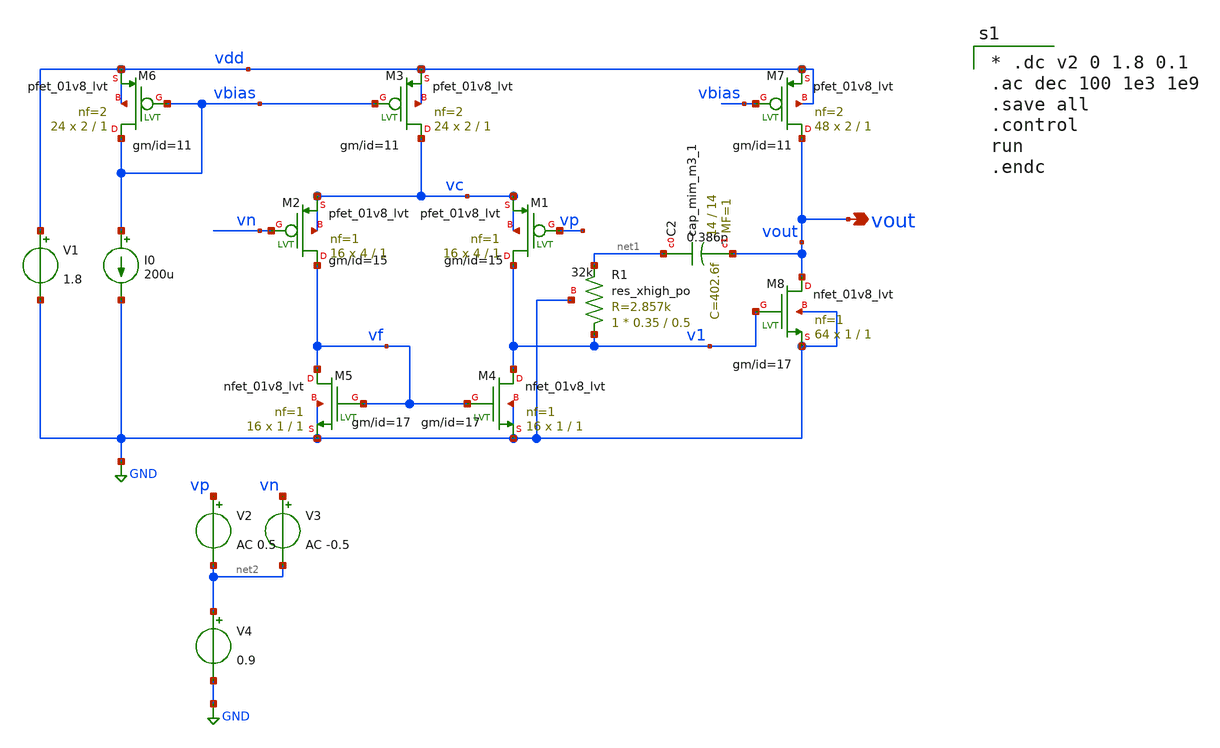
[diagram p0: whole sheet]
** sch_path: xschem/OTA_test.sch
**.subckt OTA_test vout
*.opin vout
XM1 v1 vp vc vc sky130_fd_pr__pfet_01v8_lvt L=1 W=4 nf=1 ad='int((nf+1)/2) * W/nf * 0.29' as='int((nf+2)/2) * W/nf * 0.29'
+ pd='2*int((nf+1)/2) * (W/nf + 0.29)' ps='2*int((nf+2)/2) * (W/nf + 0.29)' nrd='0.29 / W' nrs='0.29 / W'
+ sa=0 sb=0 sd=0 mult=16 m=16
XM2 vf vn vc vc sky130_fd_pr__pfet_01v8_lvt L=1 W=4 nf=1 ad='int((nf+1)/2) * W/nf * 0.29' as='int((nf+2)/2) * W/nf * 0.29'
+ pd='2*int((nf+1)/2) * (W/nf + 0.29)' ps='2*int((nf+2)/2) * (W/nf + 0.29)' nrd='0.29 / W' nrs='0.29 / W'
+ sa=0 sb=0 sd=0 mult=16 m=16
XM3 vc vbias vdd vdd sky130_fd_pr__pfet_01v8_lvt L=1 W=2 nf=2 ad='int((nf+1)/2) * W/nf * 0.29' as='int((nf+2)/2) * W/nf * 0.29'
+ pd='2*int((nf+1)/2) * (W/nf + 0.29)' ps='2*int((nf+2)/2) * (W/nf + 0.29)' nrd='0.29 / W' nrs='0.29 / W'
+ sa=0 sb=0 sd=0 mult=24 m=24
XM4 v1 vf GND GND sky130_fd_pr__nfet_01v8_lvt L=1 W=1 nf=1 ad='int((nf+1)/2) * W/nf * 0.29' as='int((nf+2)/2) * W/nf * 0.29'
+ pd='2*int((nf+1)/2) * (W/nf + 0.29)' ps='2*int((nf+2)/2) * (W/nf + 0.29)' nrd='0.29 / W' nrs='0.29 / W'
+ sa=0 sb=0 sd=0 mult=16 m=16
XM5 vf vf GND GND sky130_fd_pr__nfet_01v8_lvt L=1 W=1 nf=1 ad='int((nf+1)/2) * W/nf * 0.29' as='int((nf+2)/2) * W/nf * 0.29'
+ pd='2*int((nf+1)/2) * (W/nf + 0.29)' ps='2*int((nf+2)/2) * (W/nf + 0.29)' nrd='0.29 / W' nrs='0.29 / W'
+ sa=0 sb=0 sd=0 mult=16 m=16
XM6 vbias vbias vdd vdd sky130_fd_pr__pfet_01v8_lvt L=1 W=2 nf=2 ad='int((nf+1)/2) * W/nf * 0.29' as='int((nf+2)/2) * W/nf * 0.29'
+ pd='2*int((nf+1)/2) * (W/nf + 0.29)' ps='2*int((nf+2)/2) * (W/nf + 0.29)' nrd='0.29 / W' nrs='0.29 / W'
+ sa=0 sb=0 sd=0 mult=24 m=24
XM7 vout vbias vdd vdd sky130_fd_pr__pfet_01v8_lvt L=1 W=2 nf=2 ad='int((nf+1)/2) * W/nf * 0.29' as='int((nf+2)/2) * W/nf * 0.29'
+ pd='2*int((nf+1)/2) * (W/nf + 0.29)' ps='2*int((nf+2)/2) * (W/nf + 0.29)' nrd='0.29 / W' nrs='0.29 / W'
+ sa=0 sb=0 sd=0 mult=48 m=48
XM8 vout v1 GND GND sky130_fd_pr__nfet_01v8_lvt L=1 W=1 nf=1 ad='int((nf+1)/2) * W/nf * 0.29' as='int((nf+2)/2) * W/nf * 0.29'
+ pd='2*int((nf+1)/2) * (W/nf + 0.29)' ps='2*int((nf+2)/2) * (W/nf + 0.29)' nrd='0.29 / W' nrs='0.29 / W'
+ sa=0 sb=0 sd=0 mult=64 m=64
XR1 v1 net1 GND sky130_fd_pr__res_xhigh_po W=0.35 L=0.5 mult=1 m=1
XC2 net1 vout sky130_fd_pr__cap_mim_m3_1 W=14 L=14 MF=1 m=1
I0 vbias GND 200u
V1 vdd GND 1.8
V2 vp net2 AC 0.5
V3 vn net2 AC -0.5
V4 net2 GND 0.9
**** begin user architecture code
.lib $::SKYWATER_MODELS/sky130.lib.spice tt
.include $::PDKPATH/libs.ref/sky130_fd_sc_hs/spice/sky130_fd_sc_hs.spice


* .dc v2 0 1.8 0.1
.ac dec 100 1e3 1e9
.save all
.control
run
.endc


**** end user architecture code
**.ends
.GLOBAL GND
.end
